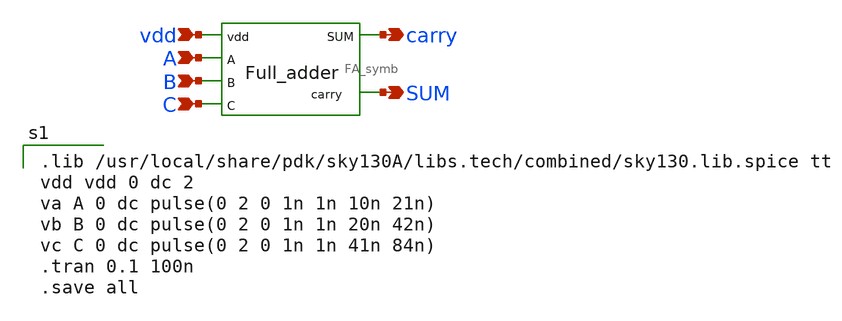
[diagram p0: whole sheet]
** sch_path: Circuit Files/circuits/circuits/FA_TB.sch
**.subckt FA_TB vdd A B C carry SUM
*.ipin vdd
*.ipin A
*.ipin B
*.ipin C
*.opin carry
*.opin SUM
x1 vdd A B SUM carry C FA_symb
**** begin user architecture code

.lib /usr/local/share/pdk/sky130A/libs.tech/combined/sky130.lib.spice tt
vdd vdd 0 dc 2
va A 0 dc pulse(0 2 0 1n 1n 10n 21n)
vb B 0 dc pulse(0 2 0 1n 1n 20n 42n)
vc C 0 dc pulse(0 2 0 1n 1n 41n 84n)
.tran 0.1 100n
.save all

**** end user architecture code
**.ends

* expanding   symbol:  daVLSI_World/Layout/FA_symb.sym # of pins=6
** sym_path: Circuit Files/circuits/circuits/FA_symb.sym
** sch_path: Circuit Files/circuits/circuits/FA_symb.sch
.subckt FA_symb vdd A B carry SUM C
*.ipin A
*.ipin B
*.ipin vdd
*.ipin C
*.opin SUM
*.opin carry
XM1 W1 A net6 GND sky130_fd_pr__nfet_01v8 L=0.15 W=W_nmos nf=1 ad='int((nf+1)/2) * W/nf * 0.29' as='int((nf+2)/2) * W/nf * 0.29'
+ pd='2*int((nf+1)/2) * (W/nf + 0.29)' ps='2*int((nf+2)/2) * (W/nf + 0.29)' nrd='0.29 / W' nrs='0.29 / W'
+ sa=0 sb=0 sd=0 mult=1 m=1
XM2 W1 Ai net7 GND sky130_fd_pr__nfet_01v8 L=0.15 W=W_nmos nf=1 ad='int((nf+1)/2) * W/nf * 0.29' as='int((nf+2)/2) * W/nf * 0.29'
+ pd='2*int((nf+1)/2) * (W/nf + 0.29)' ps='2*int((nf+2)/2) * (W/nf + 0.29)' nrd='0.29 / W' nrs='0.29 / W'
+ sa=0 sb=0 sd=0 mult=1 m=1
XM3 net6 B GND GND sky130_fd_pr__nfet_01v8 L=0.15 W=W_nmos nf=1 ad='int((nf+1)/2) * W/nf * 0.29' as='int((nf+2)/2) * W/nf * 0.29'
+ pd='2*int((nf+1)/2) * (W/nf + 0.29)' ps='2*int((nf+2)/2) * (W/nf + 0.29)' nrd='0.29 / W' nrs='0.29 / W'
+ sa=0 sb=0 sd=0 mult=1 m=1
XM4 net7 Bi GND GND sky130_fd_pr__nfet_01v8 L=0.15 W=W_nmos nf=1 ad='int((nf+1)/2) * W/nf * 0.29' as='int((nf+2)/2) * W/nf * 0.29'
+ pd='2*int((nf+1)/2) * (W/nf + 0.29)' ps='2*int((nf+2)/2) * (W/nf + 0.29)' nrd='0.29 / W' nrs='0.29 / W'
+ sa=0 sb=0 sd=0 mult=1 m=1
XM5 W1 Ai net1 vdd sky130_fd_pr__pfet_01v8 L=0.15 W=W_pmos nf=1 ad='int((nf+1)/2) * W/nf * 0.29' as='int((nf+2)/2) * W/nf * 0.29'
+ pd='2*int((nf+1)/2) * (W/nf + 0.29)' ps='2*int((nf+2)/2) * (W/nf + 0.29)' nrd='0.29 / W' nrs='0.29 / W'
+ sa=0 sb=0 sd=0 mult=1 m=1
XM6 W1 Bi net1 vdd sky130_fd_pr__pfet_01v8 L=0.15 W=W_pmos nf=1 ad='int((nf+1)/2) * W/nf * 0.29' as='int((nf+2)/2) * W/nf * 0.29'
+ pd='2*int((nf+1)/2) * (W/nf + 0.29)' ps='2*int((nf+2)/2) * (W/nf + 0.29)' nrd='0.29 / W' nrs='0.29 / W'
+ sa=0 sb=0 sd=0 mult=1 m=1
XM7 net1 A vdd vdd sky130_fd_pr__pfet_01v8 L=0.15 W=W_pmos nf=1 ad='int((nf+1)/2) * W/nf * 0.29' as='int((nf+2)/2) * W/nf * 0.29'
+ pd='2*int((nf+1)/2) * (W/nf + 0.29)' ps='2*int((nf+2)/2) * (W/nf + 0.29)' nrd='0.29 / W' nrs='0.29 / W'
+ sa=0 sb=0 sd=0 mult=1 m=1
XM8 net1 B vdd vdd sky130_fd_pr__pfet_01v8 L=0.15 W=W_pmos nf=1 ad='int((nf+1)/2) * W/nf * 0.29' as='int((nf+2)/2) * W/nf * 0.29'
+ pd='2*int((nf+1)/2) * (W/nf + 0.29)' ps='2*int((nf+2)/2) * (W/nf + 0.29)' nrd='0.29 / W' nrs='0.29 / W'
+ sa=0 sb=0 sd=0 mult=1 m=1
XM9 Ai A vdd vdd sky130_fd_pr__pfet_01v8 L=0.15 W=W_pmos nf=1 ad='int((nf+1)/2) * W/nf * 0.29' as='int((nf+2)/2) * W/nf * 0.29'
+ pd='2*int((nf+1)/2) * (W/nf + 0.29)' ps='2*int((nf+2)/2) * (W/nf + 0.29)' nrd='0.29 / W' nrs='0.29 / W'
+ sa=0 sb=0 sd=0 mult=1 m=1
XM10 Ai A GND GND sky130_fd_pr__nfet_01v8 L=0.15 W=W_nmos nf=1 ad='int((nf+1)/2) * W/nf * 0.29' as='int((nf+2)/2) * W/nf * 0.29'
+ pd='2*int((nf+1)/2) * (W/nf + 0.29)' ps='2*int((nf+2)/2) * (W/nf + 0.29)' nrd='0.29 / W' nrs='0.29 / W'
+ sa=0 sb=0 sd=0 mult=1 m=1
XM11 Bi B vdd vdd sky130_fd_pr__pfet_01v8 L=0.15 W=W_pmos nf=1 ad='int((nf+1)/2) * W/nf * 0.29' as='int((nf+2)/2) * W/nf * 0.29'
+ pd='2*int((nf+1)/2) * (W/nf + 0.29)' ps='2*int((nf+2)/2) * (W/nf + 0.29)' nrd='0.29 / W' nrs='0.29 / W'
+ sa=0 sb=0 sd=0 mult=1 m=1
XM12 Bi B GND GND sky130_fd_pr__nfet_01v8 L=0.15 W=W_nmos nf=1 ad='int((nf+1)/2) * W/nf * 0.29' as='int((nf+2)/2) * W/nf * 0.29'
+ pd='2*int((nf+1)/2) * (W/nf + 0.29)' ps='2*int((nf+2)/2) * (W/nf + 0.29)' nrd='0.29 / W' nrs='0.29 / W'
+ sa=0 sb=0 sd=0 mult=1 m=1
XM13 Ci C vdd vdd sky130_fd_pr__pfet_01v8 L=0.15 W=W_pmos nf=1 ad='int((nf+1)/2) * W/nf * 0.29' as='int((nf+2)/2) * W/nf * 0.29'
+ pd='2*int((nf+1)/2) * (W/nf + 0.29)' ps='2*int((nf+2)/2) * (W/nf + 0.29)' nrd='0.29 / W' nrs='0.29 / W'
+ sa=0 sb=0 sd=0 mult=1 m=1
XM14 Ci C GND GND sky130_fd_pr__nfet_01v8 L=0.15 W=W_nmos nf=1 ad='int((nf+1)/2) * W/nf * 0.29' as='int((nf+2)/2) * W/nf * 0.29'
+ pd='2*int((nf+1)/2) * (W/nf + 0.29)' ps='2*int((nf+2)/2) * (W/nf + 0.29)' nrd='0.29 / W' nrs='0.29 / W'
+ sa=0 sb=0 sd=0 mult=1 m=1
XM15 SUM W1 net8 GND sky130_fd_pr__nfet_01v8 L=0.15 W=W_nmos nf=1 ad='int((nf+1)/2) * W/nf * 0.29' as='int((nf+2)/2) * W/nf * 0.29'
+ pd='2*int((nf+1)/2) * (W/nf + 0.29)' ps='2*int((nf+2)/2) * (W/nf + 0.29)' nrd='0.29 / W' nrs='0.29 / W'
+ sa=0 sb=0 sd=0 mult=1 m=1
XM16 SUM W1i net9 GND sky130_fd_pr__nfet_01v8 L=0.15 W=W_nmos nf=1 ad='int((nf+1)/2) * W/nf * 0.29' as='int((nf+2)/2) * W/nf * 0.29'
+ pd='2*int((nf+1)/2) * (W/nf + 0.29)' ps='2*int((nf+2)/2) * (W/nf + 0.29)' nrd='0.29 / W' nrs='0.29 / W'
+ sa=0 sb=0 sd=0 mult=1 m=1
XM17 net8 C GND GND sky130_fd_pr__nfet_01v8 L=0.15 W=W_nmos nf=1 ad='int((nf+1)/2) * W/nf * 0.29' as='int((nf+2)/2) * W/nf * 0.29'
+ pd='2*int((nf+1)/2) * (W/nf + 0.29)' ps='2*int((nf+2)/2) * (W/nf + 0.29)' nrd='0.29 / W' nrs='0.29 / W'
+ sa=0 sb=0 sd=0 mult=1 m=1
XM18 net9 Ci GND GND sky130_fd_pr__nfet_01v8 L=0.15 W=W_nmos nf=1 ad='int((nf+1)/2) * W/nf * 0.29' as='int((nf+2)/2) * W/nf * 0.29'
+ pd='2*int((nf+1)/2) * (W/nf + 0.29)' ps='2*int((nf+2)/2) * (W/nf + 0.29)' nrd='0.29 / W' nrs='0.29 / W'
+ sa=0 sb=0 sd=0 mult=1 m=1
XM19 SUM W1i net2 vdd sky130_fd_pr__pfet_01v8 L=0.15 W=W_pmos nf=1 ad='int((nf+1)/2) * W/nf * 0.29' as='int((nf+2)/2) * W/nf * 0.29'
+ pd='2*int((nf+1)/2) * (W/nf + 0.29)' ps='2*int((nf+2)/2) * (W/nf + 0.29)' nrd='0.29 / W' nrs='0.29 / W'
+ sa=0 sb=0 sd=0 mult=1 m=1
XM20 SUM Ci net2 vdd sky130_fd_pr__pfet_01v8 L=0.15 W=W_pmos nf=1 ad='int((nf+1)/2) * W/nf * 0.29' as='int((nf+2)/2) * W/nf * 0.29'
+ pd='2*int((nf+1)/2) * (W/nf + 0.29)' ps='2*int((nf+2)/2) * (W/nf + 0.29)' nrd='0.29 / W' nrs='0.29 / W'
+ sa=0 sb=0 sd=0 mult=1 m=1
XM21 net2 W1 vdd vdd sky130_fd_pr__pfet_01v8 L=0.15 W=W_pmos nf=1 ad='int((nf+1)/2) * W/nf * 0.29' as='int((nf+2)/2) * W/nf * 0.29'
+ pd='2*int((nf+1)/2) * (W/nf + 0.29)' ps='2*int((nf+2)/2) * (W/nf + 0.29)' nrd='0.29 / W' nrs='0.29 / W'
+ sa=0 sb=0 sd=0 mult=1 m=1
XM22 net2 C vdd vdd sky130_fd_pr__pfet_01v8 L=0.15 W=W_pmos nf=1 ad='int((nf+1)/2) * W/nf * 0.29' as='int((nf+2)/2) * W/nf * 0.29'
+ pd='2*int((nf+1)/2) * (W/nf + 0.29)' ps='2*int((nf+2)/2) * (W/nf + 0.29)' nrd='0.29 / W' nrs='0.29 / W'
+ sa=0 sb=0 sd=0 mult=1 m=1
XM23 W1i W1 vdd vdd sky130_fd_pr__pfet_01v8 L=0.15 W=W_pmos nf=1 ad='int((nf+1)/2) * W/nf * 0.29' as='int((nf+2)/2) * W/nf * 0.29'
+ pd='2*int((nf+1)/2) * (W/nf + 0.29)' ps='2*int((nf+2)/2) * (W/nf + 0.29)' nrd='0.29 / W' nrs='0.29 / W'
+ sa=0 sb=0 sd=0 mult=1 m=1
XM24 W1i W1 GND GND sky130_fd_pr__nfet_01v8 L=0.15 W=W_nmos nf=1 ad='int((nf+1)/2) * W/nf * 0.29' as='int((nf+2)/2) * W/nf * 0.29'
+ pd='2*int((nf+1)/2) * (W/nf + 0.29)' ps='2*int((nf+2)/2) * (W/nf + 0.29)' nrd='0.29 / W' nrs='0.29 / W'
+ sa=0 sb=0 sd=0 mult=1 m=1
XM25 net3 A net10 GND sky130_fd_pr__nfet_01v8 L=0.15 W=W_nmos nf=1 ad='int((nf+1)/2) * W/nf * 0.29' as='int((nf+2)/2) * W/nf * 0.29'
+ pd='2*int((nf+1)/2) * (W/nf + 0.29)' ps='2*int((nf+2)/2) * (W/nf + 0.29)' nrd='0.29 / W' nrs='0.29 / W'
+ sa=0 sb=0 sd=0 mult=1 m=1
XM26 net10 B GND GND sky130_fd_pr__nfet_01v8 L=0.15 W=W_nmos nf=1 ad='int((nf+1)/2) * W/nf * 0.29' as='int((nf+2)/2) * W/nf * 0.29'
+ pd='2*int((nf+1)/2) * (W/nf + 0.29)' ps='2*int((nf+2)/2) * (W/nf + 0.29)' nrd='0.29 / W' nrs='0.29 / W'
+ sa=0 sb=0 sd=0 mult=1 m=1
XM27 net3 A vdd vdd sky130_fd_pr__pfet_01v8 L=0.15 W=W_pmos nf=1 ad='int((nf+1)/2) * W/nf * 0.29' as='int((nf+2)/2) * W/nf * 0.29'
+ pd='2*int((nf+1)/2) * (W/nf + 0.29)' ps='2*int((nf+2)/2) * (W/nf + 0.29)' nrd='0.29 / W' nrs='0.29 / W'
+ sa=0 sb=0 sd=0 mult=1 m=1
XM28 net3 B vdd vdd sky130_fd_pr__pfet_01v8 L=0.15 W=W_pmos nf=1 ad='int((nf+1)/2) * W/nf * 0.29' as='int((nf+2)/2) * W/nf * 0.29'
+ pd='2*int((nf+1)/2) * (W/nf + 0.29)' ps='2*int((nf+2)/2) * (W/nf + 0.29)' nrd='0.29 / W' nrs='0.29 / W'
+ sa=0 sb=0 sd=0 mult=1 m=1
XM31 net4 W1 net11 GND sky130_fd_pr__nfet_01v8 L=0.15 W=W_nmos nf=1 ad='int((nf+1)/2) * W/nf * 0.29'
+ as='int((nf+2)/2) * W/nf * 0.29' pd='2*int((nf+1)/2) * (W/nf + 0.29)' ps='2*int((nf+2)/2) * (W/nf + 0.29)'
+ nrd='0.29 / W' nrs='0.29 / W' sa=0 sb=0 sd=0 mult=1 m=1
XM32 net11 C GND GND sky130_fd_pr__nfet_01v8 L=0.15 W=W_nmos nf=1 ad='int((nf+1)/2) * W/nf * 0.29' as='int((nf+2)/2) * W/nf * 0.29'
+ pd='2*int((nf+1)/2) * (W/nf + 0.29)' ps='2*int((nf+2)/2) * (W/nf + 0.29)' nrd='0.29 / W' nrs='0.29 / W'
+ sa=0 sb=0 sd=0 mult=1 m=1
XM33 net4 W1 vdd vdd sky130_fd_pr__pfet_01v8 L=0.15 W=W_pmos nf=1 ad='int((nf+1)/2) * W/nf * 0.29' as='int((nf+2)/2) * W/nf * 0.29'
+ pd='2*int((nf+1)/2) * (W/nf + 0.29)' ps='2*int((nf+2)/2) * (W/nf + 0.29)' nrd='0.29 / W' nrs='0.29 / W'
+ sa=0 sb=0 sd=0 mult=1 m=1
XM34 net4 C vdd vdd sky130_fd_pr__pfet_01v8 L=0.15 W=W_pmos nf=1 ad='int((nf+1)/2) * W/nf * 0.29' as='int((nf+2)/2) * W/nf * 0.29'
+ pd='2*int((nf+1)/2) * (W/nf + 0.29)' ps='2*int((nf+2)/2) * (W/nf + 0.29)' nrd='0.29 / W' nrs='0.29 / W'
+ sa=0 sb=0 sd=0 mult=1 m=1
XM37 net5 W2 net12 vdd sky130_fd_pr__pfet_01v8 L=0.15 W=W_pmos nf=1 ad='int((nf+1)/2) * W/nf * 0.29'
+ as='int((nf+2)/2) * W/nf * 0.29' pd='2*int((nf+1)/2) * (W/nf + 0.29)' ps='2*int((nf+2)/2) * (W/nf + 0.29)'
+ nrd='0.29 / W' nrs='0.29 / W' sa=0 sb=0 sd=0 mult=1 m=1
XM38 net12 W3 vdd vdd sky130_fd_pr__pfet_01v8 L=0.15 W=W_pmos nf=1 ad='int((nf+1)/2) * W/nf * 0.29' as='int((nf+2)/2) * W/nf * 0.29'
+ pd='2*int((nf+1)/2) * (W/nf + 0.29)' ps='2*int((nf+2)/2) * (W/nf + 0.29)' nrd='0.29 / W' nrs='0.29 / W'
+ sa=0 sb=0 sd=0 mult=1 m=1
XM39 net5 W2 GND GND sky130_fd_pr__nfet_01v8 L=0.15 W=W_nmos nf=1 ad='int((nf+1)/2) * W/nf * 0.29' as='int((nf+2)/2) * W/nf * 0.29'
+ pd='2*int((nf+1)/2) * (W/nf + 0.29)' ps='2*int((nf+2)/2) * (W/nf + 0.29)' nrd='0.29 / W' nrs='0.29 / W'
+ sa=0 sb=0 sd=0 mult=1 m=1
XM40 net5 W3 GND GND sky130_fd_pr__nfet_01v8 L=0.15 W=W_nmos nf=1 ad='int((nf+1)/2) * W/nf * 0.29' as='int((nf+2)/2) * W/nf * 0.29'
+ pd='2*int((nf+1)/2) * (W/nf + 0.29)' ps='2*int((nf+2)/2) * (W/nf + 0.29)' nrd='0.29 / W' nrs='0.29 / W'
+ sa=0 sb=0 sd=0 mult=1 m=1
XM29 carry net5 vdd vdd sky130_fd_pr__pfet_01v8 L=0.15 W=W_pmos nf=1 ad='int((nf+1)/2) * W/nf * 0.29'
+ as='int((nf+2)/2) * W/nf * 0.29' pd='2*int((nf+1)/2) * (W/nf + 0.29)' ps='2*int((nf+2)/2) * (W/nf + 0.29)'
+ nrd='0.29 / W' nrs='0.29 / W' sa=0 sb=0 sd=0 mult=1 m=1
XM30 carry net5 GND GND sky130_fd_pr__nfet_01v8 L=0.15 W=W_nmos nf=1 ad='int((nf+1)/2) * W/nf * 0.29'
+ as='int((nf+2)/2) * W/nf * 0.29' pd='2*int((nf+1)/2) * (W/nf + 0.29)' ps='2*int((nf+2)/2) * (W/nf + 0.29)'
+ nrd='0.29 / W' nrs='0.29 / W' sa=0 sb=0 sd=0 mult=1 m=1
XM35 W2 net3 vdd vdd sky130_fd_pr__pfet_01v8 L=0.15 W=W_pmos nf=1 ad='int((nf+1)/2) * W/nf * 0.29' as='int((nf+2)/2) * W/nf * 0.29'
+ pd='2*int((nf+1)/2) * (W/nf + 0.29)' ps='2*int((nf+2)/2) * (W/nf + 0.29)' nrd='0.29 / W' nrs='0.29 / W'
+ sa=0 sb=0 sd=0 mult=1 m=1
XM36 W2 net3 GND GND sky130_fd_pr__nfet_01v8 L=0.15 W=W_nmos nf=1 ad='int((nf+1)/2) * W/nf * 0.29' as='int((nf+2)/2) * W/nf * 0.29'
+ pd='2*int((nf+1)/2) * (W/nf + 0.29)' ps='2*int((nf+2)/2) * (W/nf + 0.29)' nrd='0.29 / W' nrs='0.29 / W'
+ sa=0 sb=0 sd=0 mult=1 m=1
XM41 W3 net4 vdd vdd sky130_fd_pr__pfet_01v8 L=0.15 W=W_pmos nf=1 ad='int((nf+1)/2) * W/nf * 0.29' as='int((nf+2)/2) * W/nf * 0.29'
+ pd='2*int((nf+1)/2) * (W/nf + 0.29)' ps='2*int((nf+2)/2) * (W/nf + 0.29)' nrd='0.29 / W' nrs='0.29 / W'
+ sa=0 sb=0 sd=0 mult=1 m=1
XM42 W3 net4 GND GND sky130_fd_pr__nfet_01v8 L=0.15 W=W_nmos nf=1 ad='int((nf+1)/2) * W/nf * 0.29' as='int((nf+2)/2) * W/nf * 0.29'
+ pd='2*int((nf+1)/2) * (W/nf + 0.29)' ps='2*int((nf+2)/2) * (W/nf + 0.29)' nrd='0.29 / W' nrs='0.29 / W'
+ sa=0 sb=0 sd=0 mult=1 m=1
.param W_pmos=2
.param W_nmos=1
.ends

.GLOBAL GND
.end
